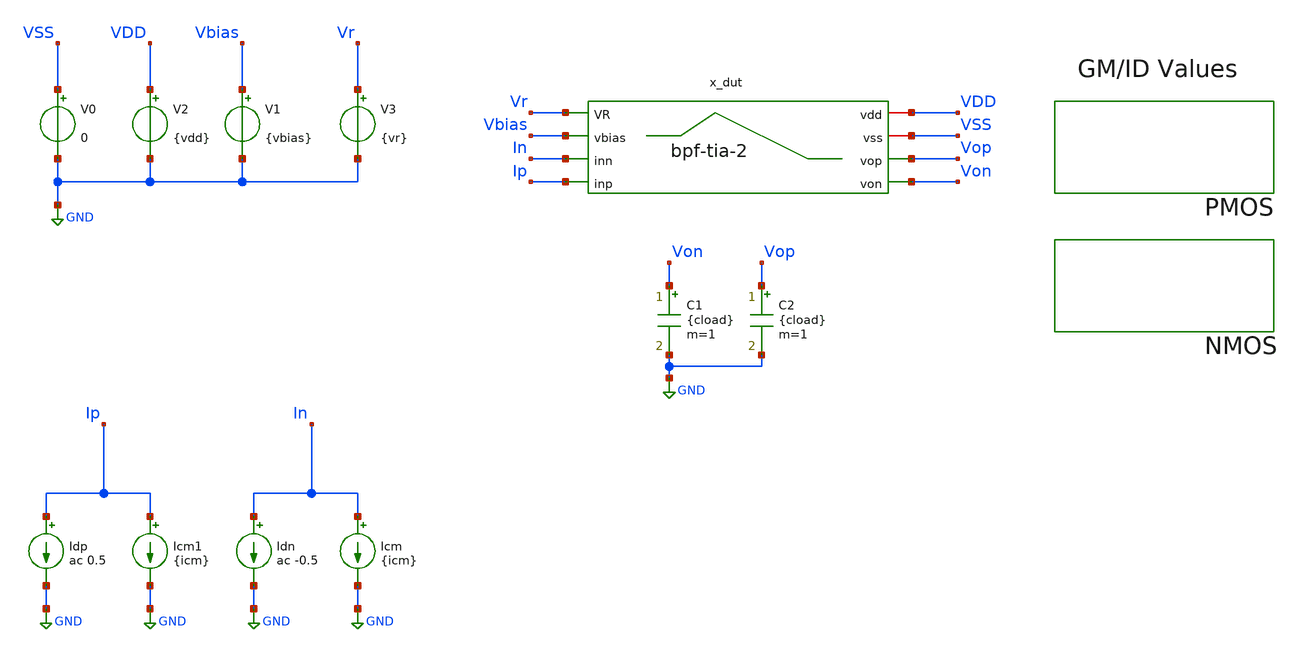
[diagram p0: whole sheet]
** sch_path: examples/tunable-tia/gf180/tia-bpf-2/tb_ac.sch
**.subckt tb_ac
V0 VSS GND 0
V2 VDD GND {vdd}
x_dut VDD VSS Vr Vop Von Vbias In Ip bpf-tia-2
V1 Vbias GND {vbias}
C1 Von GND {cload} m=1
C2 Vop GND {cload} m=1
Icm In GND {icm}
Idn In GND ac -0.5
Icm1 Ip GND {icm}
Idp Ip GND ac 0.5
V3 Vr GND {vr}
**** begin user architecture code


.control

    echo ==================================
    echo start of Control
    echo ==================================

    save all

    echo
    echo (A) start of OP
    echo ----------------------------------

    * operating point
    op
    let gm_id_1_2 = @m.x_dut.xm1.m0[gm]/@m.x_dut.xm1.m0[id]
    let gm_id_3_4 = @m.x_dut.xm3.m0[gm]/@m.x_dut.xm3.m0[id]

    print all
    write op.raw

    echo ----------------------------------
    echo END of OP
    echo ----------------------------------

    set appendwrite

    echo
    echo (B) start of AC Sim
    echo ----------------------------------

    * run ac simulation
    ac dec 200 1e1 1e12

    echo (1) post processing the AC sim
    * magnitude
    let Vout = v(Vop) - v(Von)
    let vout_mag = abs(v(Vout))
    let vout_mag_db = 20*log(vout_mag)/log(10)

    * raw phase (between -180 and 180)
    let vout_phase = phase(v(Vout)) * 180/pi

    echo (2) measuring A0, PM, UGF...

    * Bandpass response parameters
    meas ac GMAX max vout_mag
    meas ac FC when vout_mag=GMAX

    let gmax_3db = GMAX/sqrt(2)

    meas ac FLO when vout_mag=gmax_3db cross=1
    meas ac FHI when vout_mag=gmax_3db cross=2

    let BW = FHI-FLO
    let Q  = FC/BW
    let gain_db = 20 * log(GMAX) / log(10)
    print BW Q gain_db
    *meas ac A0 find vout_mag at=1k
    meas ac PM find vout_phase when vout_mag=1
    meas ac UGF when vout_mag=1 fall=1

    echo (3) plotting...
    plot vout_mag

    echo ----------------------------------
    echo END of AC sim
    echo  ----------------------------------

    echo SAVING SIMULATION RESULTS IN THE RAW FILE
    save all
    write

    echo ==================================
    echo END of Control
    echo ==================================
.endc



.include $::180MCU_MODELS/design.ngspice
.lib $::180MCU_MODELS/sm141064.ngspice typical

.lib $::180MCU_MODELS/sm141064.ngspice res_typical
* .lib $::180MCU_MODELS/sm141064.ngspice res_statistical




*.option savecurrents
* Saving gm values for transistors
.save @m.x_dut.xm1.m0[gm]
.save @m.x_dut.xm2.m0[gm]
.save @m.x_dut.xm3.m0[gm]
.save @m.x_dut.xm4.m0[gm]

* Saving id values for transistors
.save @m.x_dut.xm1.m0[id]
.save @m.x_dut.xm2.m0[id]
.save @m.x_dut.xm3.m0[id]
.save @m.x_dut.xm4.m0[id]





.param idd=1.8e-6
.param icm=0.5e-6
.param vdd=6.0

.param vbias=1.0
.param vr=1.5


.param cload=1p





* All DUT parameters

* MOSFET PARAMETERS
.param x_dut_m1_2_w=0.22u
.param x_dut_m1_2_l=0.40u
.param x_dut_m1_2_nf=2

.param x_dut_m3_4_w=0.22u
.param x_dut_m3_4_l=0.40u
.param x_dut_m3_4_nf=2

* PASSIVE ELEMENT PARAMETERS
.param x_dut_cdd=1n

.param x_dut_lss=1k


**** end user architecture code
**.ends

* expanding   symbol:  tia-bpf-2/bpf-tia-2.sym # of pins=8
** sym_path: examples/tunable-tia/gf180/tia-bpf-2/bpf-tia-2.sym
** sch_path: examples/tunable-tia/gf180/tia-bpf-2/bpf-tia-2.sch
.subckt bpf-tia-2 vdd vss VR vop von vbias inn inp
*.iopin vdd
*.iopin vss
*.ipin inp
*.ipin inn
*.opin von
*.opin vop
*.ipin vbias
*.ipin VR
XM1 von vbias inp vss nfet_03v3 L={x_dut_m1_2_l} W={x_dut_m1_2_w} nf=1 ad='int((nf+1)/2) * W/nf * 0.18u'
+ as='int((nf+2)/2) * W/nf * 0.18u' pd='2*int((nf+1)/2) * (W/nf + 0.18u)' ps='2*int((nf+2)/2) * (W/nf + 0.18u)'
+ nrd='0.18u / W' nrs='0.18u / W' sa=0 sb=0 sd=0 m=1
XM2 vop vbias inn vss nfet_03v3 L={x_dut_m1_2_l} W={x_dut_m1_2_w} nf=1 ad='int((nf+1)/2) * W/nf * 0.18u'
+ as='int((nf+2)/2) * W/nf * 0.18u' pd='2*int((nf+1)/2) * (W/nf + 0.18u)' ps='2*int((nf+2)/2) * (W/nf + 0.18u)'
+ nrd='0.18u / W' nrs='0.18u / W' sa=0 sb=0 sd=0 m=1
C1 vdd von {x_dut_cdd} m=1
C2 vdd vop {x_dut_cdd} m=1
XM3 von VR vdd vdd pfet_03v3 L={x_dut_m3_4_l} W={x_dut_m3_4_w} nf=1 ad='int((nf+1)/2) * W/nf * 0.18u'
+ as='int((nf+2)/2) * W/nf * 0.18u' pd='2*int((nf+1)/2) * (W/nf + 0.18u)' ps='2*int((nf+2)/2) * (W/nf + 0.18u)'
+ nrd='0.18u / W' nrs='0.18u / W' sa=0 sb=0 sd=0 m=1
XM4 vop VR vdd vdd pfet_03v3 L={x_dut_m3_4_l} W={x_dut_m3_4_w} nf=1 ad='int((nf+1)/2) * W/nf * 0.18u'
+ as='int((nf+2)/2) * W/nf * 0.18u' pd='2*int((nf+1)/2) * (W/nf + 0.18u)' ps='2*int((nf+2)/2) * (W/nf + 0.18u)'
+ nrd='0.18u / W' nrs='0.18u / W' sa=0 sb=0 sd=0 m=1
L2 inp vss {x_dut_lss} m=1
L3 inn vss {x_dut_lss} m=1
.ends

.GLOBAL GND
.end
